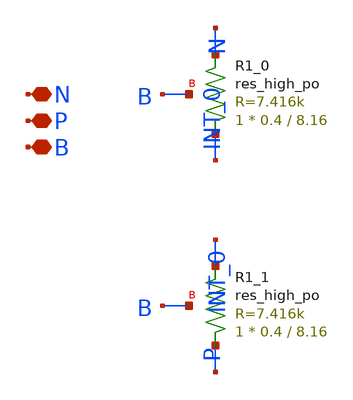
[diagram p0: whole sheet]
** sch_path: design/LELO_TEMP_SKY130A/REYATR_RES_36C2F0.sch
**.subckt REYATR_RES_36C2F0 N P B
*.iopin N
*.iopin P
*.iopin B
XR1_0 INT_0 N B sky130_fd_pr__res_high_po W=0.4 L=8.16 mult=1 m=1
XR1_1 P INT_0 B sky130_fd_pr__res_high_po W=0.4 L=8.16 mult=1 m=1
**.ends
.end
